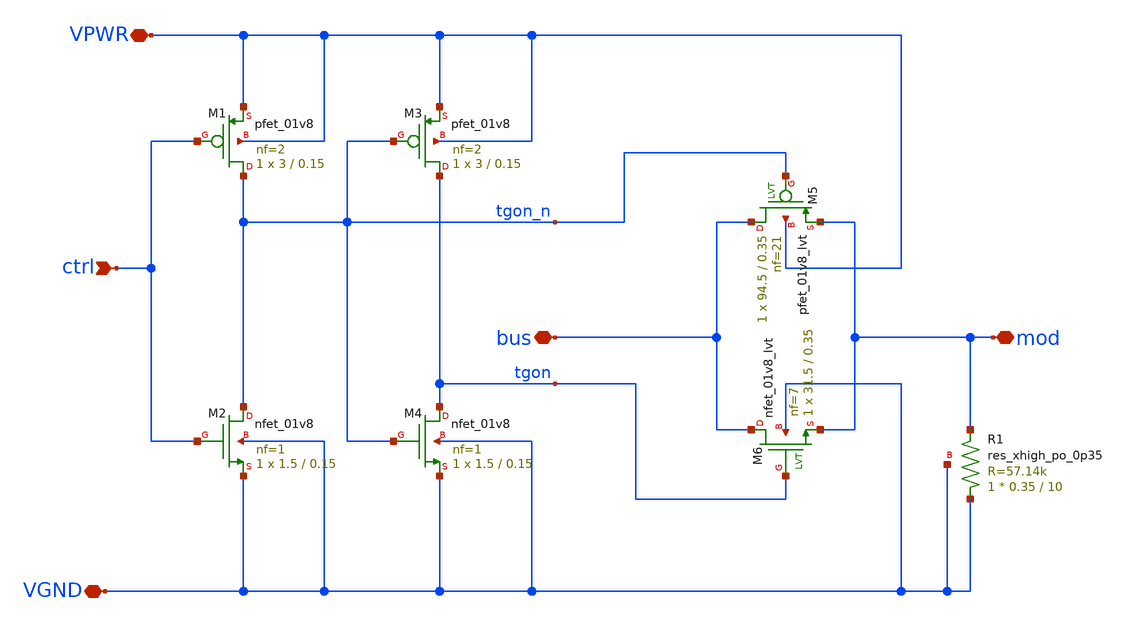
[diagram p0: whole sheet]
** sch_path: xschem/analog_mux.sch
**.subckt analog_mux VPWR VGND mod bus ctrl
*.iopin VPWR
*.iopin VGND
*.iopin mod
*.iopin bus
*.ipin ctrl
XM4 tgon tgon_n VGND VGND sky130_fd_pr__nfet_01v8 L=0.15 W=1.5 nf=1 ad='int((nf+1)/2) * W/nf * 0.29'
+ as='int((nf+2)/2) * W/nf * 0.29' pd='2*int((nf+1)/2) * (W/nf + 0.29)' ps='2*int((nf+2)/2) * (W/nf + 0.29)'
+ nrd='0.29 / W' nrs='0.29 / W' sa=0 sb=0 sd=0 mult=1 m=1
XM3 tgon tgon_n VPWR VPWR sky130_fd_pr__pfet_01v8 L=0.15 W=3 nf=2 ad='int((nf+1)/2) * W/nf * 0.29' as='int((nf+2)/2) * W/nf * 0.29'
+ pd='2*int((nf+1)/2) * (W/nf + 0.29)' ps='2*int((nf+2)/2) * (W/nf + 0.29)' nrd='0.29 / W' nrs='0.29 / W'
+ sa=0 sb=0 sd=0 mult=1 m=1
XM2 tgon_n ctrl VGND VGND sky130_fd_pr__nfet_01v8 L=0.15 W=1.5 nf=1 ad='int((nf+1)/2) * W/nf * 0.29'
+ as='int((nf+2)/2) * W/nf * 0.29' pd='2*int((nf+1)/2) * (W/nf + 0.29)' ps='2*int((nf+2)/2) * (W/nf + 0.29)'
+ nrd='0.29 / W' nrs='0.29 / W' sa=0 sb=0 sd=0 mult=1 m=1
XM1 tgon_n ctrl VPWR VPWR sky130_fd_pr__pfet_01v8 L=0.15 W=3 nf=2 ad='int((nf+1)/2) * W/nf * 0.29' as='int((nf+2)/2) * W/nf * 0.29'
+ pd='2*int((nf+1)/2) * (W/nf + 0.29)' ps='2*int((nf+2)/2) * (W/nf + 0.29)' nrd='0.29 / W' nrs='0.29 / W'
+ sa=0 sb=0 sd=0 mult=1 m=1
XM6 bus tgon mod VGND sky130_fd_pr__nfet_01v8_lvt L=0.35 W=31.5 nf=7 ad='int((nf+1)/2) * W/nf * 0.29'
+ as='int((nf+2)/2) * W/nf * 0.29' pd='2*int((nf+1)/2) * (W/nf + 0.29)' ps='2*int((nf+2)/2) * (W/nf + 0.29)'
+ nrd='0.29 / W' nrs='0.29 / W' sa=0 sb=0 sd=0 mult=1 m=1
XM5 bus tgon_n mod VPWR sky130_fd_pr__pfet_01v8_lvt L=0.35 W=94.5 nf=21 ad='int((nf+1)/2) * W/nf * 0.29'
+ as='int((nf+2)/2) * W/nf * 0.29' pd='2*int((nf+1)/2) * (W/nf + 0.29)' ps='2*int((nf+2)/2) * (W/nf + 0.29)'
+ nrd='0.29 / W' nrs='0.29 / W' sa=0 sb=0 sd=0 mult=1 m=1
XR1 VGND mod VGND sky130_fd_pr__res_xhigh_po_0p35 L=10 mult=1 m=1
**.ends
.end
